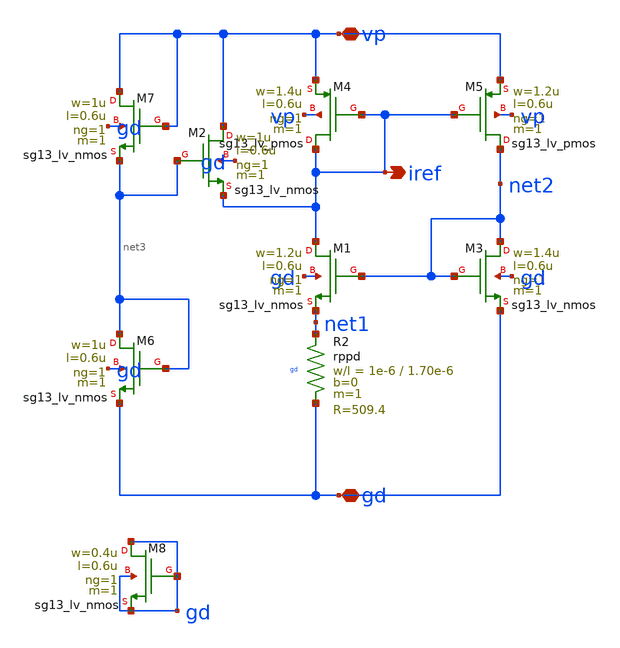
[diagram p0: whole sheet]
** sch_path: charge_pump/curr_source.sch
**.subckt curr_source vp gd iref
*.iopin vp
*.iopin gd
*.opin iref
XM4 iref iref vp vp sg13_lv_pmos w=1.4u l=0.6u ng=1 m=1 mm_ok=1
XM5 net2 iref vp vp sg13_lv_pmos w=1.2u l=0.6u ng=1 m=1 mm_ok=1
XM6 net3 net3 gd gd sg13_lv_nmos w=1u l=0.6u ng=1 m=1 mm_ok=1
XM3 net2 net2 gd gd sg13_lv_nmos w=1.4u l=0.6u ng=1 m=1 mm_ok=1
XR2 net1 gd gd rppd w=1e-6 l=1.70e-6 m=1 b=0 mm_ok=1
XM1 iref net2 net1 gd sg13_lv_nmos w=1.2u l=0.6u ng=1 m=1 mm_ok=1
XM2 vp net3 iref gd sg13_lv_nmos w=1u l=0.6u ng=1 m=1 mm_ok=1
XM7 vp vp net3 gd sg13_lv_nmos w=1u l=0.6u ng=1 m=1 mm_ok=1
XM8 gd gd gd gd sg13_lv_nmos w=0.4u l=0.6u ng=1 m=1 mm_ok=1
**.ends
.end
